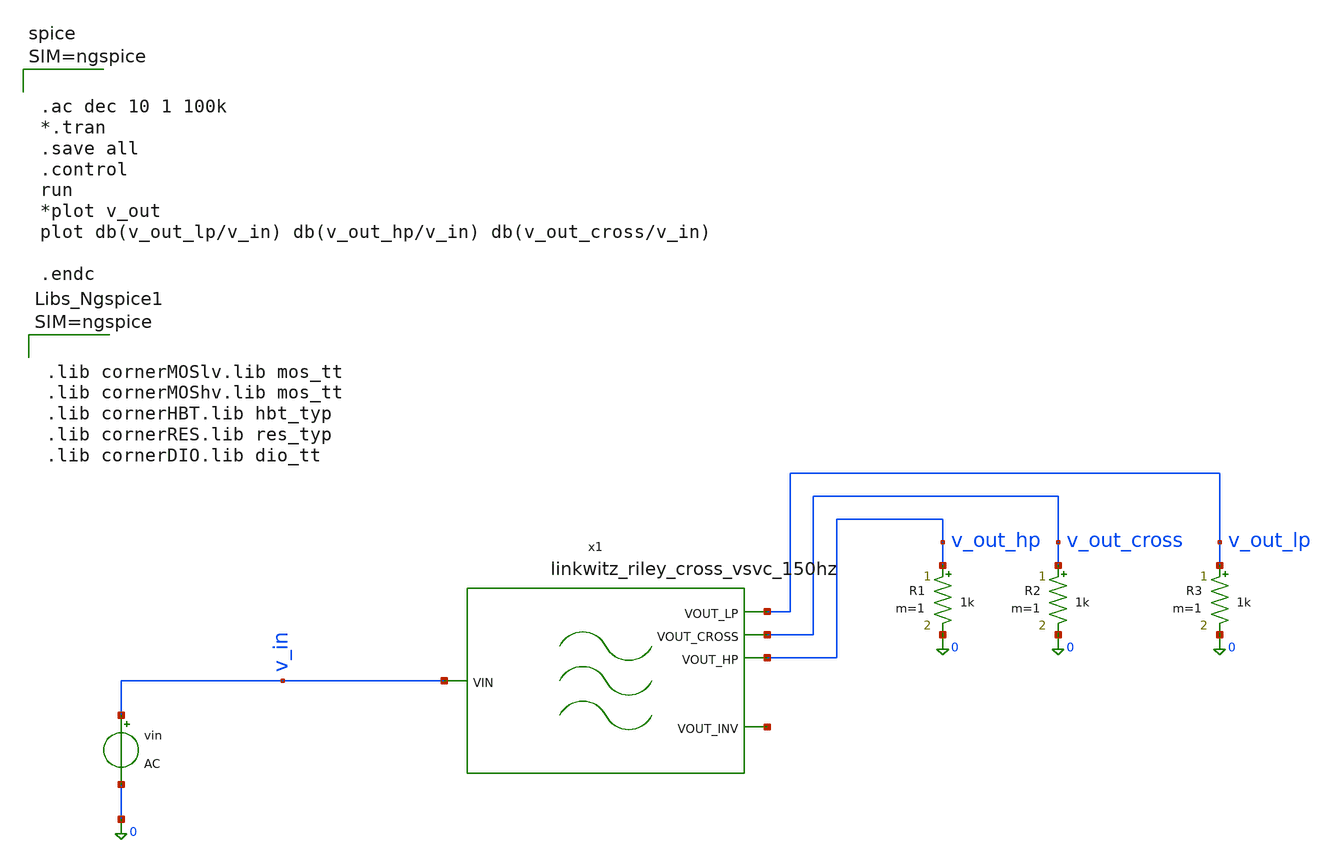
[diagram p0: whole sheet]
** sch_path: 003_Ideal_Circuits/linkwitz_riley_top_tb.sch
**.subckt linkwitz_riley_top_tb
vin v_in 0 AC
R1 v_out_hp 0 1k m=1
R2 v_out_cross 0 1k m=1
R3 v_out_lp 0 1k m=1
x1 v_out_lp v_out_cross v_in net1 v_out_hp linkwitz_riley_cross_vsvc_150hz
**** begin user architecture code



.lib cornerMOSlv.lib mos_tt
.lib cornerMOShv.lib mos_tt
.lib cornerHBT.lib hbt_typ
.lib cornerRES.lib res_typ
.lib cornerDIO.lib dio_tt






.ac dec 10 1 100k
*.tran
.save all
.control
run
*plot v_out
plot db(v_out_lp/v_in) db(v_out_hp/v_in) db(v_out_cross/v_in)

.endc



**** end user architecture code
**.ends

* expanding   symbol:  /foss/designs/Repo/003_Ideal_Circuits/linkwitz_riley_cross_vsvc_150hz.sym #
*+ of pins=5
** sym_path: 003_Ideal_Circuits/linkwitz_riley_cross_vsvc_150hz.sym
** sch_path: 003_Ideal_Circuits/linkwitz_riley_cross_vsvc_150hz.sch
.subckt linkwitz_riley_cross_vsvc_150hz VOUT_LP VOUT_CROSS VIN VOUT_INV VOUT_HP
*.ipin VIN
*.opin VOUT_LP
*.opin VOUT_HP
*.opin VOUT_INV
*.opin VOUT_CROSS
R1 net1 VIN R_LP m=1
R2 net2 net1 R_LP m=1
C1 net1 VOUT_LP C_LP m=1
C2 net2 0 C_LP m=1
.param C_LP=1.06e-6
.param R_LP=1000
R3 0 net4 R_HP m=1
R4 net3 VOUT_HP R_HP m=1
C3 net3 net4 C_HP m=1
C4 VIN net3 C_HP m=1
.param C_HP=1e-9
.param R_HP=1.06e6
R5 net5 VOUT_INV R_IN m=1
R6 VOUT_HP net5 R_IN m=1
.param R_IN=1k
R7 net6 VOUT_CROSS R_IN m=1
R8 VOUT_INV net6 R_IN m=1
R9 VOUT_LP net6 R_IN m=1
E2 VOUT_LP 0 net2 VOUT_LP 1e6
E1 VOUT_HP 0 net4 VOUT_HP 1e6
E3 VOUT_INV 0 0 net5 1e6
E4 VOUT_CROSS 0 0 net6 1e6
.ends

.end
